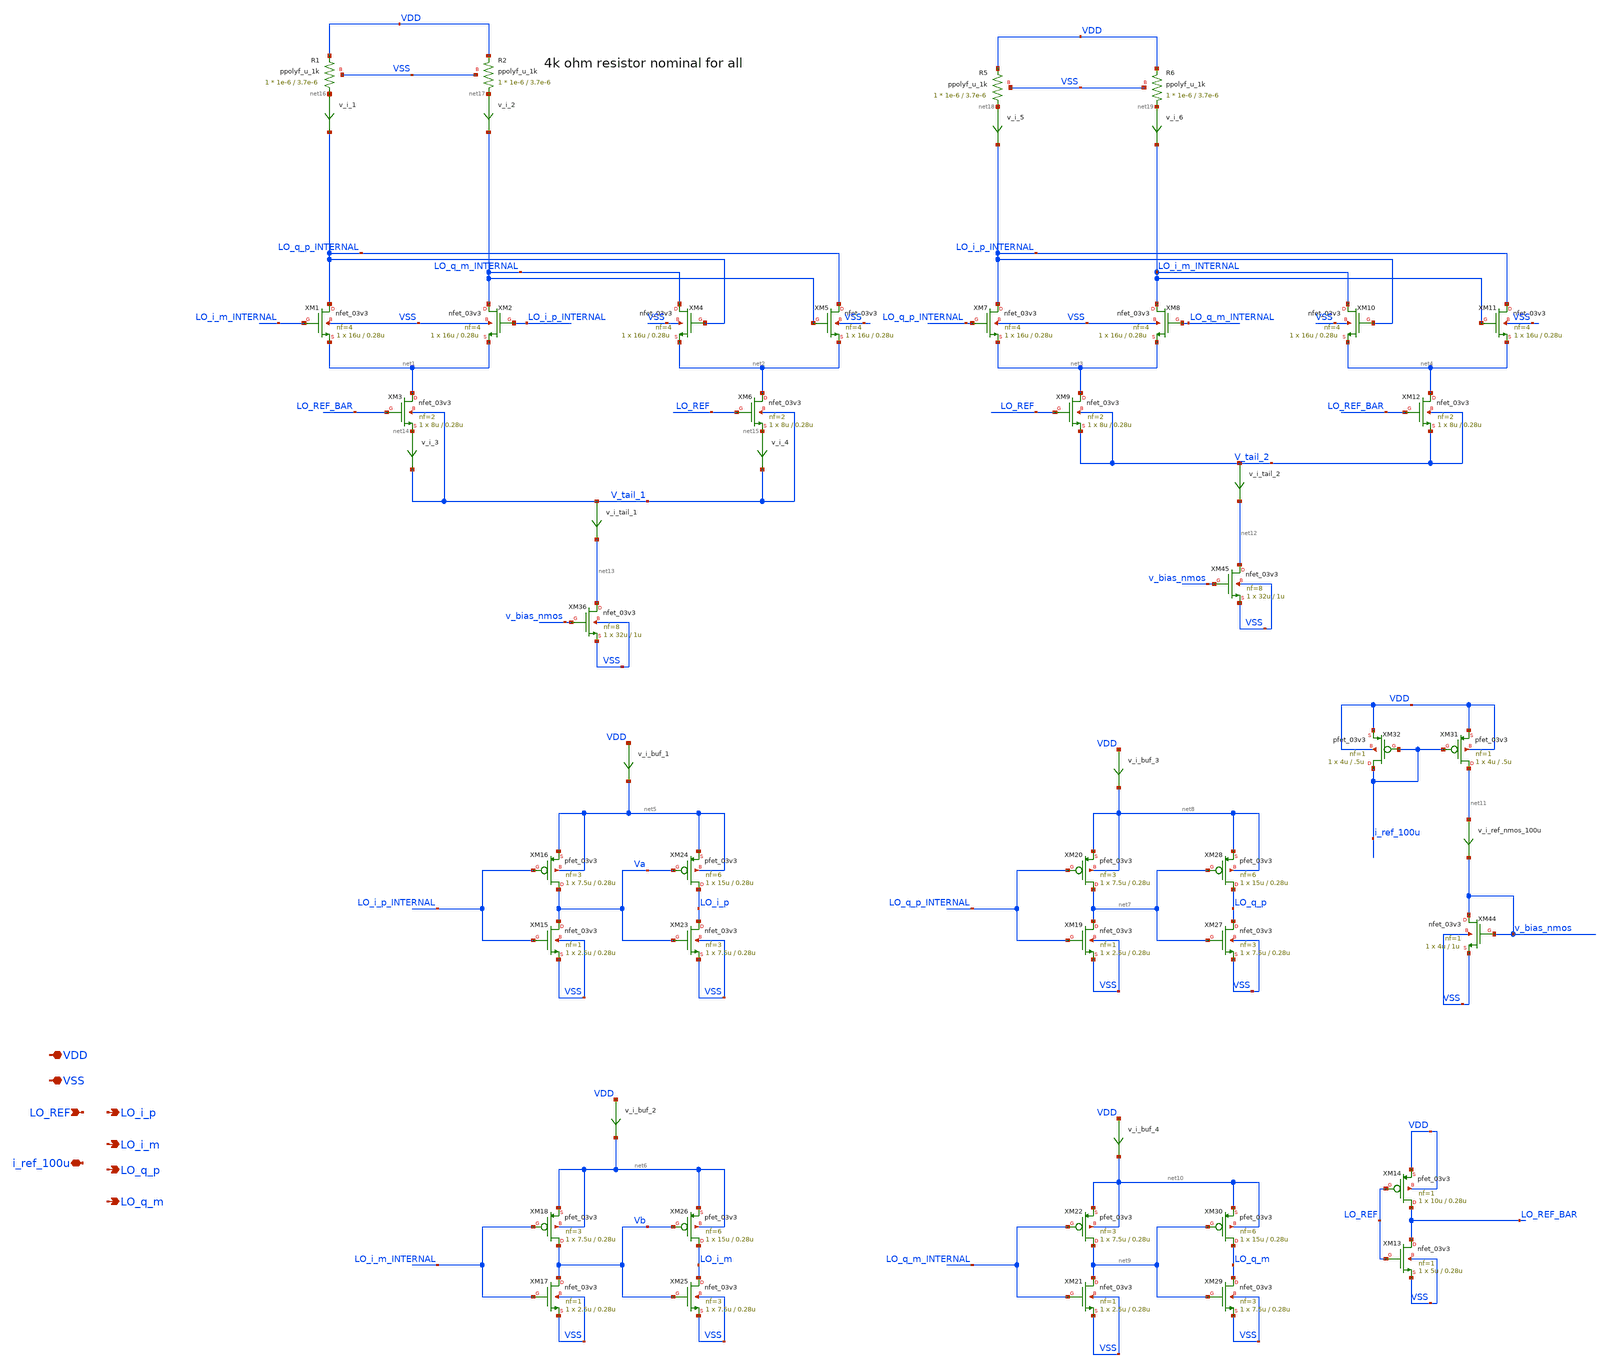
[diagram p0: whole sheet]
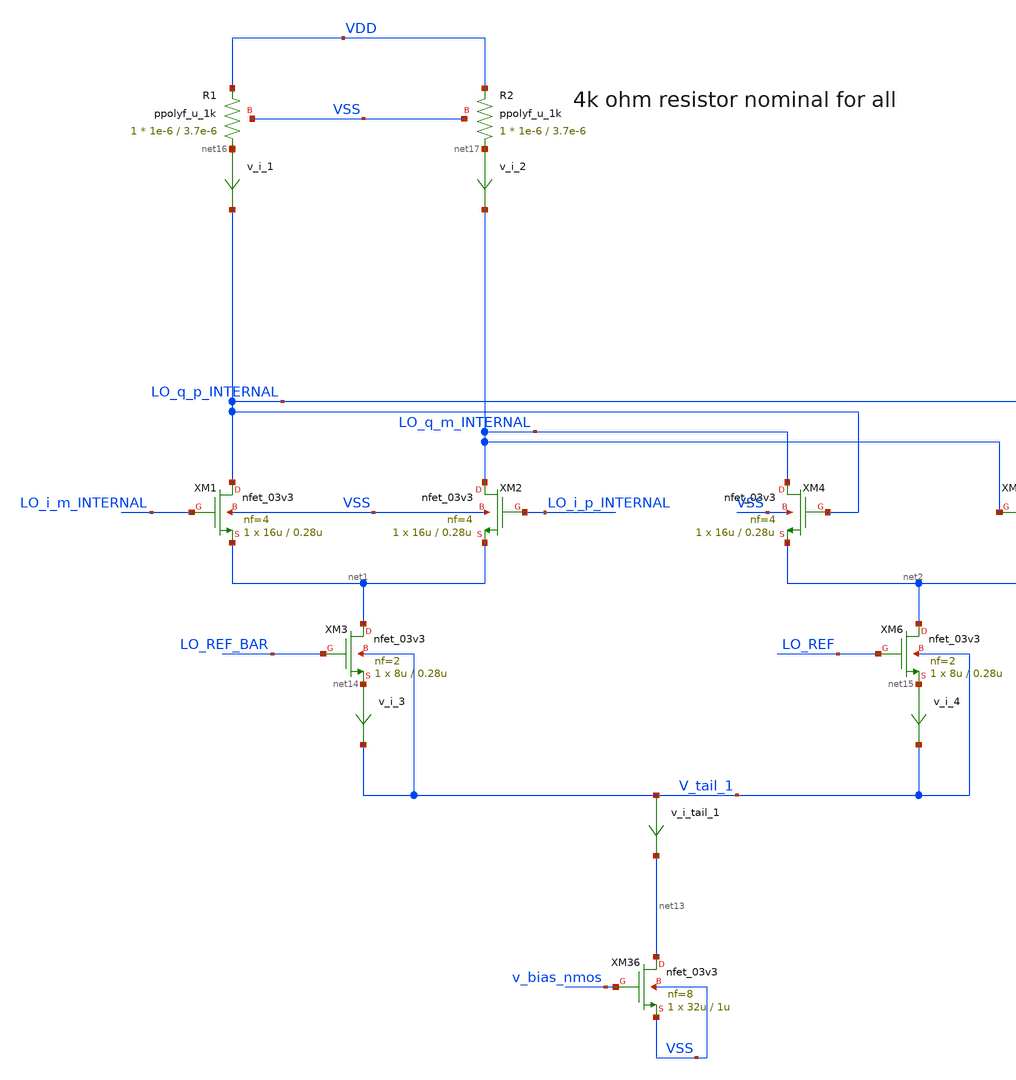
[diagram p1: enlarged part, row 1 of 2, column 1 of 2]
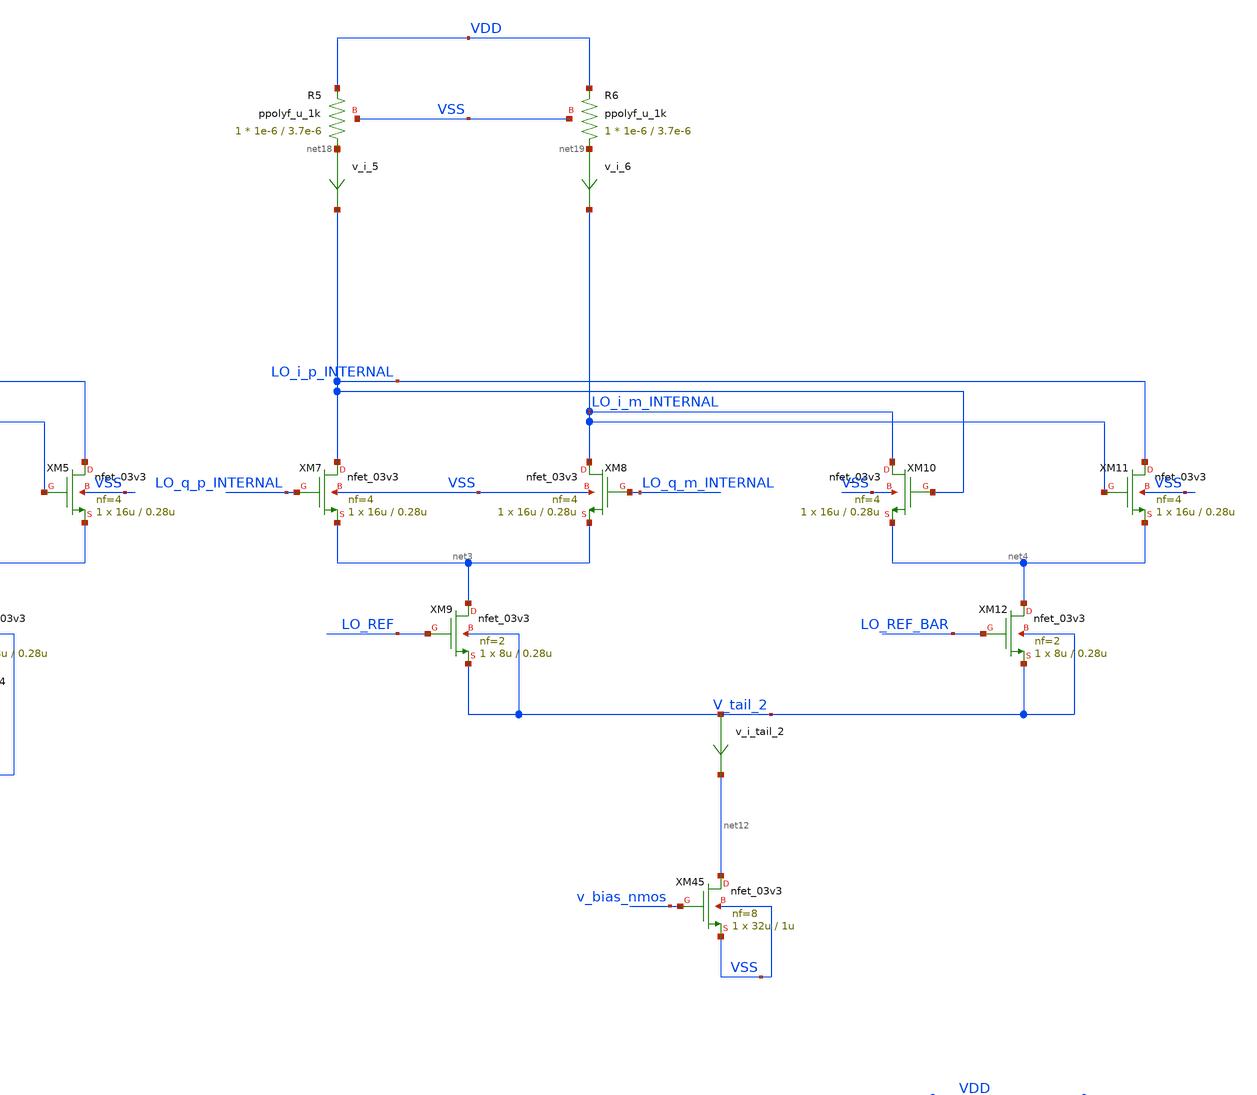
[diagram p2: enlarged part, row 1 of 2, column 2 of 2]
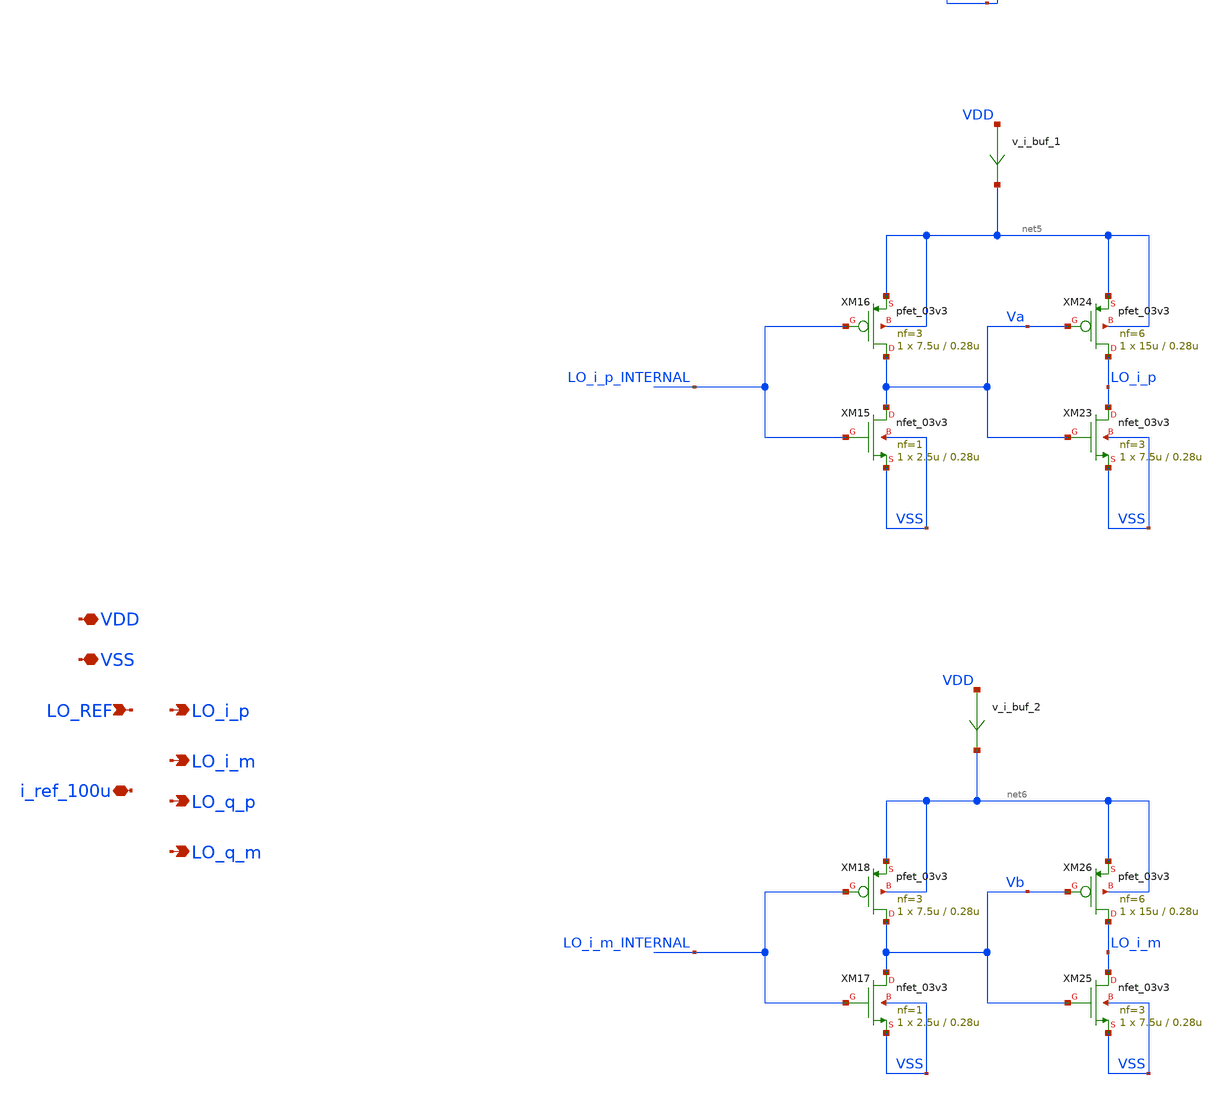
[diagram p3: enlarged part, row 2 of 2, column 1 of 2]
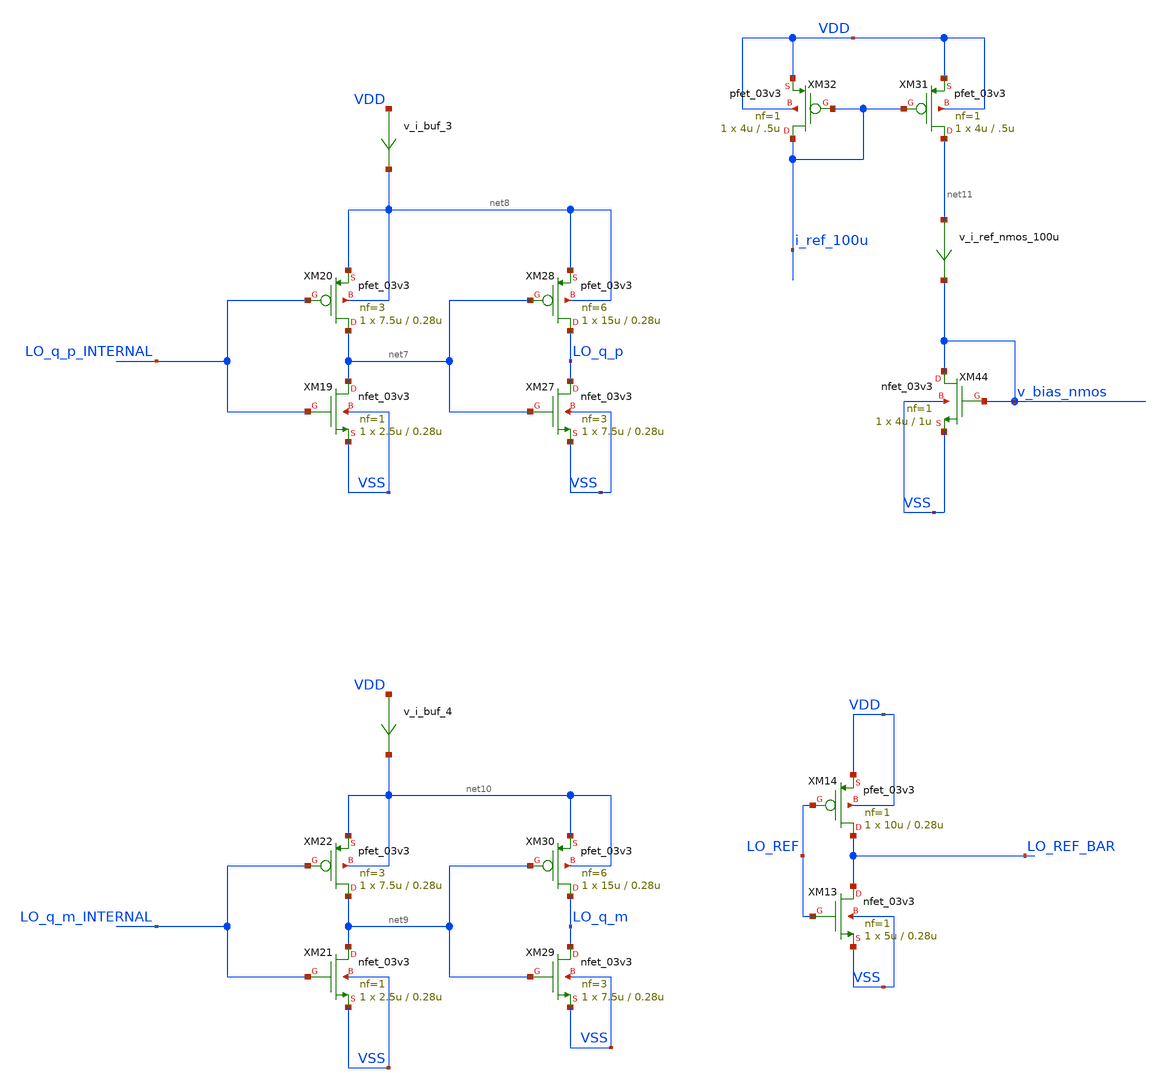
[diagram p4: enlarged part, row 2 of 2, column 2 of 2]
** sch_path: designs/divider/schematic/divider_with_tail.sch
**.subckt divider_with_tail VDD VSS LO_REF LO_i_p LO_i_m LO_q_p LO_q_m i_ref_100u
*.iopin VDD
*.iopin VSS
*.ipin LO_REF
*.opin LO_i_p
*.opin LO_i_m
*.opin LO_q_p
*.opin LO_q_m
*.iopin i_ref_100u
XM1 LO_q_p_INTERNAL LO_i_m_INTERNAL net1 VSS nfet_03v3 L=0.28u W=16u nf=4 ad='int((nf+1)/2) * W/nf * 0.18u'
+ as='int((nf+2)/2) * W/nf * 0.18u' pd='2*int((nf+1)/2) * (W/nf + 0.18u)' ps='2*int((nf+2)/2) * (W/nf + 0.18u)'
+ nrd='0.18u / W' nrs='0.18u / W' sa=0 sb=0 sd=0 m=1
XM2 LO_q_m_INTERNAL LO_i_p_INTERNAL net1 VSS nfet_03v3 L=0.28u W=16u nf=4 ad='int((nf+1)/2) * W/nf * 0.18u'
+ as='int((nf+2)/2) * W/nf * 0.18u' pd='2*int((nf+1)/2) * (W/nf + 0.18u)' ps='2*int((nf+2)/2) * (W/nf + 0.18u)'
+ nrd='0.18u / W' nrs='0.18u / W' sa=0 sb=0 sd=0 m=1
XM3 net1 LO_REF_BAR net14 V_tail_1 nfet_03v3 L=0.28u W=8u nf=2 ad='int((nf+1)/2) * W/nf * 0.18u' as='int((nf+2)/2) * W/nf * 0.18u'
+ pd='2*int((nf+1)/2) * (W/nf + 0.18u)' ps='2*int((nf+2)/2) * (W/nf + 0.18u)' nrd='0.18u / W' nrs='0.18u / W'
+ sa=0 sb=0 sd=0 m=1
XM4 LO_q_m_INTERNAL LO_q_p_INTERNAL net2 VSS nfet_03v3 L=0.28u W=16u nf=4 ad='int((nf+1)/2) * W/nf * 0.18u'
+ as='int((nf+2)/2) * W/nf * 0.18u' pd='2*int((nf+1)/2) * (W/nf + 0.18u)' ps='2*int((nf+2)/2) * (W/nf + 0.18u)'
+ nrd='0.18u / W' nrs='0.18u / W' sa=0 sb=0 sd=0 m=1
XM5 LO_q_p_INTERNAL LO_q_m_INTERNAL net2 VSS nfet_03v3 L=0.28u W=16u nf=4 ad='int((nf+1)/2) * W/nf * 0.18u'
+ as='int((nf+2)/2) * W/nf * 0.18u' pd='2*int((nf+1)/2) * (W/nf + 0.18u)' ps='2*int((nf+2)/2) * (W/nf + 0.18u)'
+ nrd='0.18u / W' nrs='0.18u / W' sa=0 sb=0 sd=0 m=1
XM6 net2 LO_REF net15 V_tail_1 nfet_03v3 L=0.28u W=8u nf=2 ad='int((nf+1)/2) * W/nf * 0.18u' as='int((nf+2)/2) * W/nf * 0.18u'
+ pd='2*int((nf+1)/2) * (W/nf + 0.18u)' ps='2*int((nf+2)/2) * (W/nf + 0.18u)' nrd='0.18u / W' nrs='0.18u / W'
+ sa=0 sb=0 sd=0 m=1
XM7 LO_i_p_INTERNAL LO_q_p_INTERNAL net3 VSS nfet_03v3 L=0.28u W=16u nf=4 ad='int((nf+1)/2) * W/nf * 0.18u'
+ as='int((nf+2)/2) * W/nf * 0.18u' pd='2*int((nf+1)/2) * (W/nf + 0.18u)' ps='2*int((nf+2)/2) * (W/nf + 0.18u)'
+ nrd='0.18u / W' nrs='0.18u / W' sa=0 sb=0 sd=0 m=1
XM8 LO_i_m_INTERNAL LO_q_m_INTERNAL net3 VSS nfet_03v3 L=0.28u W=16u nf=4 ad='int((nf+1)/2) * W/nf * 0.18u'
+ as='int((nf+2)/2) * W/nf * 0.18u' pd='2*int((nf+1)/2) * (W/nf + 0.18u)' ps='2*int((nf+2)/2) * (W/nf + 0.18u)'
+ nrd='0.18u / W' nrs='0.18u / W' sa=0 sb=0 sd=0 m=1
XM9 net3 LO_REF V_tail_2 V_tail_2 nfet_03v3 L=0.28u W=8u nf=2 ad='int((nf+1)/2) * W/nf * 0.18u' as='int((nf+2)/2) * W/nf * 0.18u'
+ pd='2*int((nf+1)/2) * (W/nf + 0.18u)' ps='2*int((nf+2)/2) * (W/nf + 0.18u)' nrd='0.18u / W' nrs='0.18u / W'
+ sa=0 sb=0 sd=0 m=1
XM10 LO_i_m_INTERNAL LO_i_p_INTERNAL net4 VSS nfet_03v3 L=0.28u W=16u nf=4 ad='int((nf+1)/2) * W/nf * 0.18u'
+ as='int((nf+2)/2) * W/nf * 0.18u' pd='2*int((nf+1)/2) * (W/nf + 0.18u)' ps='2*int((nf+2)/2) * (W/nf + 0.18u)'
+ nrd='0.18u / W' nrs='0.18u / W' sa=0 sb=0 sd=0 m=1
XM11 LO_i_p_INTERNAL LO_i_m_INTERNAL net4 VSS nfet_03v3 L=0.28u W=16u nf=4 ad='int((nf+1)/2) * W/nf * 0.18u'
+ as='int((nf+2)/2) * W/nf * 0.18u' pd='2*int((nf+1)/2) * (W/nf + 0.18u)' ps='2*int((nf+2)/2) * (W/nf + 0.18u)'
+ nrd='0.18u / W' nrs='0.18u / W' sa=0 sb=0 sd=0 m=1
XM12 net4 LO_REF_BAR V_tail_2 V_tail_2 nfet_03v3 L=0.28u W=8u nf=2 ad='int((nf+1)/2) * W/nf * 0.18u'
+ as='int((nf+2)/2) * W/nf * 0.18u' pd='2*int((nf+1)/2) * (W/nf + 0.18u)' ps='2*int((nf+2)/2) * (W/nf + 0.18u)'
+ nrd='0.18u / W' nrs='0.18u / W' sa=0 sb=0 sd=0 m=1
XM13 LO_REF_BAR LO_REF VSS VSS nfet_03v3 L=0.28u W=5u nf=1 ad='int((nf+1)/2) * W/nf * 0.18u' as='int((nf+2)/2) * W/nf * 0.18u'
+ pd='2*int((nf+1)/2) * (W/nf + 0.18u)' ps='2*int((nf+2)/2) * (W/nf + 0.18u)' nrd='0.18u / W' nrs='0.18u / W'
+ sa=0 sb=0 sd=0 m=1
XM14 LO_REF_BAR LO_REF VDD VDD pfet_03v3 L=0.28u W=10u nf=1 ad='int((nf+1)/2) * W/nf * 0.18u' as='int((nf+2)/2) * W/nf * 0.18u'
+ pd='2*int((nf+1)/2) * (W/nf + 0.18u)' ps='2*int((nf+2)/2) * (W/nf + 0.18u)' nrd='0.18u / W' nrs='0.18u / W'
+ sa=0 sb=0 sd=0 m=1
XM15 Va LO_i_p_INTERNAL VSS VSS nfet_03v3 L=0.28u W=2.5u nf=1 ad='int((nf+1)/2) * W/nf * 0.18u' as='int((nf+2)/2) * W/nf * 0.18u'
+ pd='2*int((nf+1)/2) * (W/nf + 0.18u)' ps='2*int((nf+2)/2) * (W/nf + 0.18u)' nrd='0.18u / W' nrs='0.18u / W'
+ sa=0 sb=0 sd=0 m=1
XM16 Va LO_i_p_INTERNAL net5 net5 pfet_03v3 L=0.28u W=7.5u nf=3 ad='int((nf+1)/2) * W/nf * 0.18u' as='int((nf+2)/2) * W/nf * 0.18u'
+ pd='2*int((nf+1)/2) * (W/nf + 0.18u)' ps='2*int((nf+2)/2) * (W/nf + 0.18u)' nrd='0.18u / W' nrs='0.18u / W'
+ sa=0 sb=0 sd=0 m=1
XM17 Vb LO_i_m_INTERNAL VSS VSS nfet_03v3 L=0.28u W=2.5u nf=1 ad='int((nf+1)/2) * W/nf * 0.18u' as='int((nf+2)/2) * W/nf * 0.18u'
+ pd='2*int((nf+1)/2) * (W/nf + 0.18u)' ps='2*int((nf+2)/2) * (W/nf + 0.18u)' nrd='0.18u / W' nrs='0.18u / W'
+ sa=0 sb=0 sd=0 m=1
XM18 Vb LO_i_m_INTERNAL net6 net6 pfet_03v3 L=0.28u W=7.5u nf=3 ad='int((nf+1)/2) * W/nf * 0.18u' as='int((nf+2)/2) * W/nf * 0.18u'
+ pd='2*int((nf+1)/2) * (W/nf + 0.18u)' ps='2*int((nf+2)/2) * (W/nf + 0.18u)' nrd='0.18u / W' nrs='0.18u / W'
+ sa=0 sb=0 sd=0 m=1
XM19 net7 LO_q_p_INTERNAL VSS VSS nfet_03v3 L=0.28u W=2.5u nf=1 ad='int((nf+1)/2) * W/nf * 0.18u' as='int((nf+2)/2) * W/nf * 0.18u'
+ pd='2*int((nf+1)/2) * (W/nf + 0.18u)' ps='2*int((nf+2)/2) * (W/nf + 0.18u)' nrd='0.18u / W' nrs='0.18u / W'
+ sa=0 sb=0 sd=0 m=1
XM20 net7 LO_q_p_INTERNAL net8 net8 pfet_03v3 L=0.28u W=7.5u nf=3 ad='int((nf+1)/2) * W/nf * 0.18u' as='int((nf+2)/2) * W/nf * 0.18u'
+ pd='2*int((nf+1)/2) * (W/nf + 0.18u)' ps='2*int((nf+2)/2) * (W/nf + 0.18u)' nrd='0.18u / W' nrs='0.18u / W'
+ sa=0 sb=0 sd=0 m=1
XM21 net9 LO_q_m_INTERNAL VSS VSS nfet_03v3 L=0.28u W=2.5u nf=1 ad='int((nf+1)/2) * W/nf * 0.18u' as='int((nf+2)/2) * W/nf * 0.18u'
+ pd='2*int((nf+1)/2) * (W/nf + 0.18u)' ps='2*int((nf+2)/2) * (W/nf + 0.18u)' nrd='0.18u / W' nrs='0.18u / W'
+ sa=0 sb=0 sd=0 m=1
XM22 net9 LO_q_m_INTERNAL net10 net10 pfet_03v3 L=0.28u W=7.5u nf=3 ad='int((nf+1)/2) * W/nf * 0.18u'
+ as='int((nf+2)/2) * W/nf * 0.18u' pd='2*int((nf+1)/2) * (W/nf + 0.18u)' ps='2*int((nf+2)/2) * (W/nf + 0.18u)'
+ nrd='0.18u / W' nrs='0.18u / W' sa=0 sb=0 sd=0 m=1
XM24 LO_i_p Va net5 net5 pfet_03v3 L=0.28u W=15u nf=6 ad='int((nf+1)/2) * W/nf * 0.18u' as='int((nf+2)/2) * W/nf * 0.18u'
+ pd='2*int((nf+1)/2) * (W/nf + 0.18u)' ps='2*int((nf+2)/2) * (W/nf + 0.18u)' nrd='0.18u / W' nrs='0.18u / W'
+ sa=0 sb=0 sd=0 m=1
XM26 LO_i_m Vb net6 net6 pfet_03v3 L=0.28u W=15u nf=6 ad='int((nf+1)/2) * W/nf * 0.18u' as='int((nf+2)/2) * W/nf * 0.18u'
+ pd='2*int((nf+1)/2) * (W/nf + 0.18u)' ps='2*int((nf+2)/2) * (W/nf + 0.18u)' nrd='0.18u / W' nrs='0.18u / W'
+ sa=0 sb=0 sd=0 m=1
XM28 LO_q_p net7 net8 net8 pfet_03v3 L=0.28u W=15u nf=6 ad='int((nf+1)/2) * W/nf * 0.18u' as='int((nf+2)/2) * W/nf * 0.18u'
+ pd='2*int((nf+1)/2) * (W/nf + 0.18u)' ps='2*int((nf+2)/2) * (W/nf + 0.18u)' nrd='0.18u / W' nrs='0.18u / W'
+ sa=0 sb=0 sd=0 m=1
XM30 LO_q_m net9 net10 net10 pfet_03v3 L=0.28u W=15u nf=6 ad='int((nf+1)/2) * W/nf * 0.18u' as='int((nf+2)/2) * W/nf * 0.18u'
+ pd='2*int((nf+1)/2) * (W/nf + 0.18u)' ps='2*int((nf+2)/2) * (W/nf + 0.18u)' nrd='0.18u / W' nrs='0.18u / W'
+ sa=0 sb=0 sd=0 m=1
XM23 LO_i_p Va VSS VSS nfet_03v3 L=0.28u W=7.5u nf=3 ad='int((nf+1)/2) * W/nf * 0.18u' as='int((nf+2)/2) * W/nf * 0.18u'
+ pd='2*int((nf+1)/2) * (W/nf + 0.18u)' ps='2*int((nf+2)/2) * (W/nf + 0.18u)' nrd='0.18u / W' nrs='0.18u / W'
+ sa=0 sb=0 sd=0 m=1
XM25 LO_i_m Vb VSS VSS nfet_03v3 L=0.28u W=7.5u nf=3 ad='int((nf+1)/2) * W/nf * 0.18u' as='int((nf+2)/2) * W/nf * 0.18u'
+ pd='2*int((nf+1)/2) * (W/nf + 0.18u)' ps='2*int((nf+2)/2) * (W/nf + 0.18u)' nrd='0.18u / W' nrs='0.18u / W'
+ sa=0 sb=0 sd=0 m=1
XM27 LO_q_p net7 VSS VSS nfet_03v3 L=0.28u W=7.5u nf=3 ad='int((nf+1)/2) * W/nf * 0.18u' as='int((nf+2)/2) * W/nf * 0.18u'
+ pd='2*int((nf+1)/2) * (W/nf + 0.18u)' ps='2*int((nf+2)/2) * (W/nf + 0.18u)' nrd='0.18u / W' nrs='0.18u / W'
+ sa=0 sb=0 sd=0 m=1
XM29 LO_q_m net9 VSS VSS nfet_03v3 L=0.28u W=7.5u nf=3 ad='int((nf+1)/2) * W/nf * 0.18u' as='int((nf+2)/2) * W/nf * 0.18u'
+ pd='2*int((nf+1)/2) * (W/nf + 0.18u)' ps='2*int((nf+2)/2) * (W/nf + 0.18u)' nrd='0.18u / W' nrs='0.18u / W'
+ sa=0 sb=0 sd=0 m=1
XM44 v_bias_nmos v_bias_nmos VSS VSS nfet_03v3 L=1u W=4u nf=1 ad='int((nf+1)/2) * W/nf * 0.18u' as='int((nf+2)/2) * W/nf * 0.18u'
+ pd='2*int((nf+1)/2) * (W/nf + 0.18u)' ps='2*int((nf+2)/2) * (W/nf + 0.18u)' nrd='0.18u / W' nrs='0.18u / W'
+ sa=0 sb=0 sd=0 m=1
XM45 net12 v_bias_nmos VSS VSS nfet_03v3 L=1u W=32u nf=8 ad='int((nf+1)/2) * W/nf * 0.18u' as='int((nf+2)/2) * W/nf * 0.18u'
+ pd='2*int((nf+1)/2) * (W/nf + 0.18u)' ps='2*int((nf+2)/2) * (W/nf + 0.18u)' nrd='0.18u / W' nrs='0.18u / W'
+ sa=0 sb=0 sd=0 m=1
v_i_ref_nmos_100u net11 v_bias_nmos 0
.save i(v_i_ref_nmos_100u)
v_i_3 net14 V_tail_1 0
.save i(v_i_3)
v_i_4 net15 V_tail_1 0
.save i(v_i_4)
v_i_1 net16 LO_q_p_INTERNAL 0
.save i(v_i_1)
v_i_2 net17 LO_q_m_INTERNAL 0
.save i(v_i_2)
v_i_buf_1 VDD net5 0
.save i(v_i_buf_1)
v_i_buf_2 VDD net6 0
.save i(v_i_buf_2)
v_i_tail_2 V_tail_2 net12 0
.save i(v_i_tail_2)
XM36 net13 v_bias_nmos VSS VSS nfet_03v3 L=1u W=32u nf=8 ad='int((nf+1)/2) * W/nf * 0.18u' as='int((nf+2)/2) * W/nf * 0.18u'
+ pd='2*int((nf+1)/2) * (W/nf + 0.18u)' ps='2*int((nf+2)/2) * (W/nf + 0.18u)' nrd='0.18u / W' nrs='0.18u / W'
+ sa=0 sb=0 sd=0 m=1
v_i_tail_1 V_tail_1 net13 0
.save i(v_i_tail_1)
XM31 net11 i_ref_100u VDD VDD pfet_03v3 L=.5u W=4u nf=1 ad='int((nf+1)/2) * W/nf * 0.18u' as='int((nf+2)/2) * W/nf * 0.18u'
+ pd='2*int((nf+1)/2) * (W/nf + 0.18u)' ps='2*int((nf+2)/2) * (W/nf + 0.18u)' nrd='0.18u / W' nrs='0.18u / W'
+ sa=0 sb=0 sd=0 m=1
XM32 i_ref_100u i_ref_100u VDD VDD pfet_03v3 L=.5u W=4u nf=1 ad='int((nf+1)/2) * W/nf * 0.18u' as='int((nf+2)/2) * W/nf * 0.18u'
+ pd='2*int((nf+1)/2) * (W/nf + 0.18u)' ps='2*int((nf+2)/2) * (W/nf + 0.18u)' nrd='0.18u / W' nrs='0.18u / W'
+ sa=0 sb=0 sd=0 m=1
v_i_buf_3 VDD net8 0
.save i(v_i_buf_3)
v_i_buf_4 VDD net10 0
.save i(v_i_buf_4)
v_i_5 net18 LO_i_p_INTERNAL 0
.save i(v_i_5)
v_i_6 net19 LO_i_m_INTERNAL 0
.save i(v_i_6)
XR1 net16 VDD VSS ppolyf_u_1k r_width=1e-6 r_length=3.7e-6 m=1
XR2 net17 VDD VSS ppolyf_u_1k r_width=1e-6 r_length=3.7e-6 m=1
XR5 net18 VDD VSS ppolyf_u_1k r_width=1e-6 r_length=3.7e-6 m=1
XR6 net19 VDD VSS ppolyf_u_1k r_width=1e-6 r_length=3.7e-6 m=1
**.ends
.end
